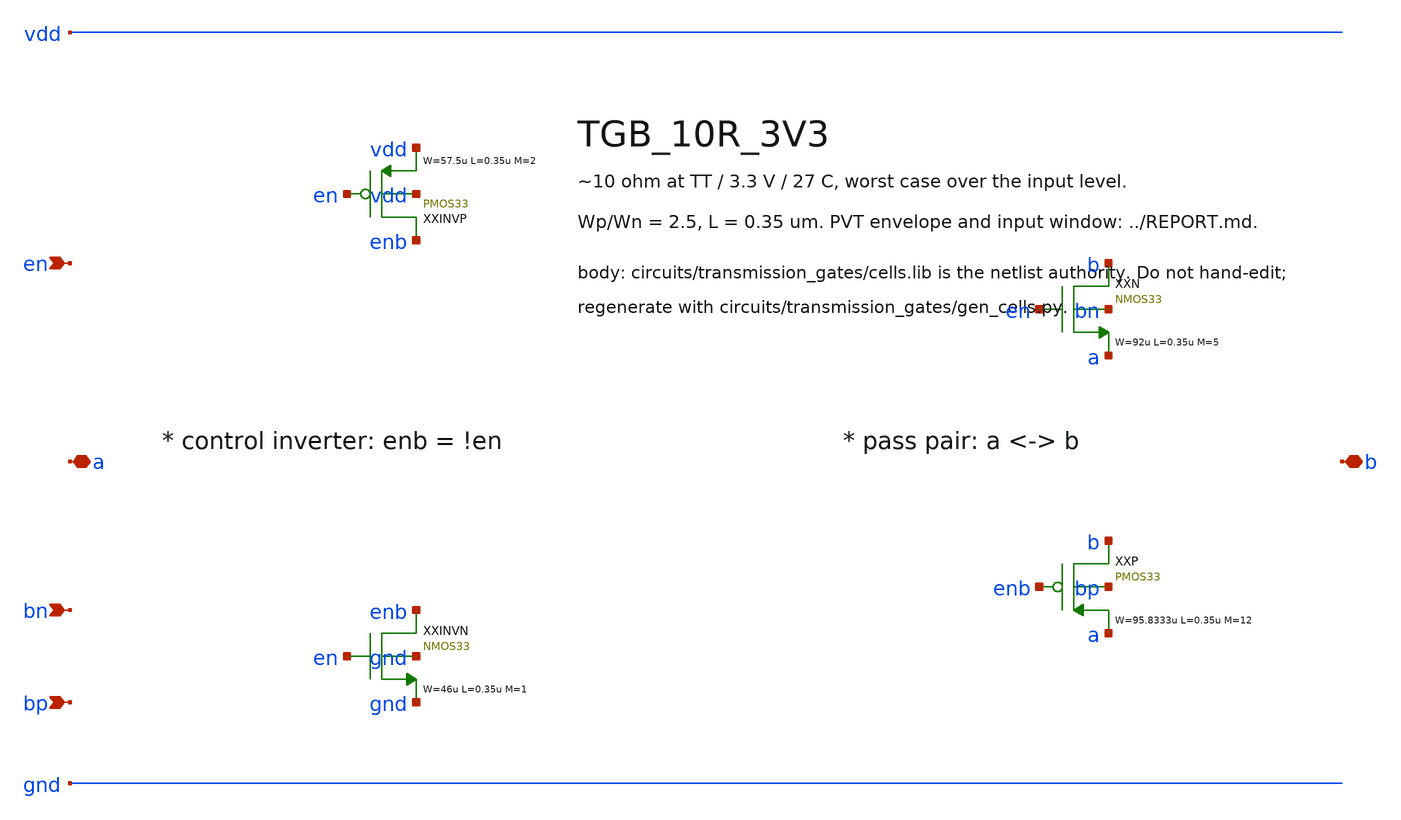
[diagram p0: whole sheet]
** sch_path: xschem/transmission_gates/TGB_10R_3V3.sch
**.subckt TGB_10R_3V3 a b en bn bp
*.iopin a
*.iopin b
*.ipin en
*.ipin bn
*.ipin bp
XXINVP enb en vdd vdd PMOS33 W=57.5u L=0.35u M=2 MM_SIGMA=0
XXINVN enb en gnd gnd NMOS33 W=46u L=0.35u M=1 MM_SIGMA=0
XXN b en a bn NMOS33 W=92u L=0.35u M=5 MM_SIGMA=0
XXP b enb a bp PMOS33 W=95.8333u L=0.35u M=12 MM_SIGMA=0
**.ends
.end
